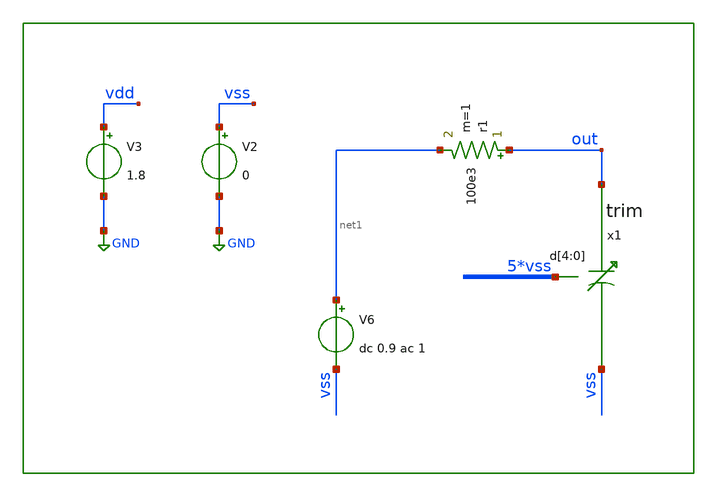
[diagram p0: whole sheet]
** sch_path: xschem/tb/comparator/ac_trim.sch
**.subckt ac_trim
V2 vss GND 0
V3 vdd GND 1.8
V6 net1 vss dc 0.9 ac 1
r1 out net1 100e3 m=1
x1 out vss vss vss vss vss vss trim
**** begin user architecture code

.param MC_SWITCH=0

.control
save all
ac dec 10 1 1e9

meas ac fbw when vdb(out)=-3
let ctrim = 1/(2*3.14159265*fbw*100e3)

print fbw
print ctrim

.endc


 * FET CORNERS
.include $::SKYWATER_MODELS/corners/tt.spice
*.include $::SKYWATER_MODELS/corners/ff.spice
*.include $::SKYWATER_MODELS/corners/ss.spice
*.include $::SKYWATER_MODELS/corners/sf.spice
*.include $::SKYWATER_MODELS/corners/fs.spice

* TT + R + C
*.include $::SKYWATER_MODELS/corners/tt_rmax_cmax.spice
*.include $::SKYWATER_MODELS/corners/tt_rmin_cmin.spice
*.include $::SKYWATER_MODELS/corners/tt_rmax_cmin.spice
*.include $::SKYWATER_MODELS/corners/tt_rmin_cmax.spice

* FF + R + C
*.include $::SKYWATER_MODELS/corners/ff_rmax_cmax.spice
*.include $::SKYWATER_MODELS/corners/ff_rmin_cmin.spice
*.include $::SKYWATER_MODELS/corners/ff_rmax_cmin.spice
*.include $::SKYWATER_MODELS/corners/ff_rmin_cmax.spice


* SS + R + C
*.include $::SKYWATER_MODELS/corners/ss_rmax_cmax.spice
*.include $::SKYWATER_MODELS/corners/ss_rmin_cmin.spice
*.include $::SKYWATER_MODELS/corners/ss_rmax_cmin.spice
*.include $::SKYWATER_MODELS/corners/ss_rmin_cmax.spice

* SF + R + C
*.include $::SKYWATER_MODELS/corners/sf_rmax_cmax.spice
*.include $::SKYWATER_MODELS/corners/sf_rmin_cmin.spice
*.include $::SKYWATER_MODELS/corners/sf_rmax_cmin.spice
*.include $::SKYWATER_MODELS/corners/sf_rmin_cmax.spice

* FS + R + C
*.include $::SKYWATER_MODELS/corners/fs_rmax_cmax.spice
*.include $::SKYWATER_MODELS/corners/fs_rmin_cmin.spice
*.include $::SKYWATER_MODELS/corners/fs_rmax_cmin.spice
*.include $::SKYWATER_MODELS/corners/fs_rmin_cmax.spice

**** end user architecture code
**.ends

* expanding   symbol:  sar_10b/comparator/trim.sym # of pins=3
** sym_path: xschem/sar_10b/comparator/trim.sym
** sch_path: xschem/sar_10b/comparator/trim.sch
.subckt trim drain d[4] d[3] d[2] d[1] d[0] vss
*.iopin vss
*.ipin d[4],d[3],d[2],d[1],d[0]
*.opin drain
XM4[7] n4 d[4] vss vss sky130_fd_pr__nfet_01v8_lvt L=0.3 W=1 nf=1 ad='int((nf+1)/2) * W/nf * 0.29' as='int((nf+2)/2) * W/nf * 0.29'
+ pd='2*int((nf+1)/2) * (W/nf + 0.29)' ps='2*int((nf+2)/2) * (W/nf + 0.29)' nrd='0.29 / W' nrs='0.29 / W'
+ sa=0 sb=0 sd=0 mult=1 m=1
XM4[6] n4 d[4] vss vss sky130_fd_pr__nfet_01v8_lvt L=0.3 W=1 nf=1 ad='int((nf+1)/2) * W/nf * 0.29' as='int((nf+2)/2) * W/nf * 0.29'
+ pd='2*int((nf+1)/2) * (W/nf + 0.29)' ps='2*int((nf+2)/2) * (W/nf + 0.29)' nrd='0.29 / W' nrs='0.29 / W'
+ sa=0 sb=0 sd=0 mult=1 m=1
XM4[5] n4 d[4] vss vss sky130_fd_pr__nfet_01v8_lvt L=0.3 W=1 nf=1 ad='int((nf+1)/2) * W/nf * 0.29' as='int((nf+2)/2) * W/nf * 0.29'
+ pd='2*int((nf+1)/2) * (W/nf + 0.29)' ps='2*int((nf+2)/2) * (W/nf + 0.29)' nrd='0.29 / W' nrs='0.29 / W'
+ sa=0 sb=0 sd=0 mult=1 m=1
XM4[4] n4 d[4] vss vss sky130_fd_pr__nfet_01v8_lvt L=0.3 W=1 nf=1 ad='int((nf+1)/2) * W/nf * 0.29' as='int((nf+2)/2) * W/nf * 0.29'
+ pd='2*int((nf+1)/2) * (W/nf + 0.29)' ps='2*int((nf+2)/2) * (W/nf + 0.29)' nrd='0.29 / W' nrs='0.29 / W'
+ sa=0 sb=0 sd=0 mult=1 m=1
XM4[3] n4 d[4] vss vss sky130_fd_pr__nfet_01v8_lvt L=0.3 W=1 nf=1 ad='int((nf+1)/2) * W/nf * 0.29' as='int((nf+2)/2) * W/nf * 0.29'
+ pd='2*int((nf+1)/2) * (W/nf + 0.29)' ps='2*int((nf+2)/2) * (W/nf + 0.29)' nrd='0.29 / W' nrs='0.29 / W'
+ sa=0 sb=0 sd=0 mult=1 m=1
XM4[2] n4 d[4] vss vss sky130_fd_pr__nfet_01v8_lvt L=0.3 W=1 nf=1 ad='int((nf+1)/2) * W/nf * 0.29' as='int((nf+2)/2) * W/nf * 0.29'
+ pd='2*int((nf+1)/2) * (W/nf + 0.29)' ps='2*int((nf+2)/2) * (W/nf + 0.29)' nrd='0.29 / W' nrs='0.29 / W'
+ sa=0 sb=0 sd=0 mult=1 m=1
XM4[1] n4 d[4] vss vss sky130_fd_pr__nfet_01v8_lvt L=0.3 W=1 nf=1 ad='int((nf+1)/2) * W/nf * 0.29' as='int((nf+2)/2) * W/nf * 0.29'
+ pd='2*int((nf+1)/2) * (W/nf + 0.29)' ps='2*int((nf+2)/2) * (W/nf + 0.29)' nrd='0.29 / W' nrs='0.29 / W'
+ sa=0 sb=0 sd=0 mult=1 m=1
XM4[0] n4 d[4] vss vss sky130_fd_pr__nfet_01v8_lvt L=0.3 W=1 nf=1 ad='int((nf+1)/2) * W/nf * 0.29' as='int((nf+2)/2) * W/nf * 0.29'
+ pd='2*int((nf+1)/2) * (W/nf + 0.29)' ps='2*int((nf+2)/2) * (W/nf + 0.29)' nrd='0.29 / W' nrs='0.29 / W'
+ sa=0 sb=0 sd=0 mult=1 m=1
XM3[3] n3 d[3] vss vss sky130_fd_pr__nfet_01v8_lvt L=0.3 W=1 nf=1 ad='int((nf+1)/2) * W/nf * 0.29' as='int((nf+2)/2) * W/nf * 0.29'
+ pd='2*int((nf+1)/2) * (W/nf + 0.29)' ps='2*int((nf+2)/2) * (W/nf + 0.29)' nrd='0.29 / W' nrs='0.29 / W'
+ sa=0 sb=0 sd=0 mult=1 m=1
XM3[2] n3 d[3] vss vss sky130_fd_pr__nfet_01v8_lvt L=0.3 W=1 nf=1 ad='int((nf+1)/2) * W/nf * 0.29' as='int((nf+2)/2) * W/nf * 0.29'
+ pd='2*int((nf+1)/2) * (W/nf + 0.29)' ps='2*int((nf+2)/2) * (W/nf + 0.29)' nrd='0.29 / W' nrs='0.29 / W'
+ sa=0 sb=0 sd=0 mult=1 m=1
XM3[1] n3 d[3] vss vss sky130_fd_pr__nfet_01v8_lvt L=0.3 W=1 nf=1 ad='int((nf+1)/2) * W/nf * 0.29' as='int((nf+2)/2) * W/nf * 0.29'
+ pd='2*int((nf+1)/2) * (W/nf + 0.29)' ps='2*int((nf+2)/2) * (W/nf + 0.29)' nrd='0.29 / W' nrs='0.29 / W'
+ sa=0 sb=0 sd=0 mult=1 m=1
XM3[0] n3 d[3] vss vss sky130_fd_pr__nfet_01v8_lvt L=0.3 W=1 nf=1 ad='int((nf+1)/2) * W/nf * 0.29' as='int((nf+2)/2) * W/nf * 0.29'
+ pd='2*int((nf+1)/2) * (W/nf + 0.29)' ps='2*int((nf+2)/2) * (W/nf + 0.29)' nrd='0.29 / W' nrs='0.29 / W'
+ sa=0 sb=0 sd=0 mult=1 m=1
XM2[1] n2 d[2] vss vss sky130_fd_pr__nfet_01v8_lvt L=0.3 W=1 nf=1 ad='int((nf+1)/2) * W/nf * 0.29' as='int((nf+2)/2) * W/nf * 0.29'
+ pd='2*int((nf+1)/2) * (W/nf + 0.29)' ps='2*int((nf+2)/2) * (W/nf + 0.29)' nrd='0.29 / W' nrs='0.29 / W'
+ sa=0 sb=0 sd=0 mult=1 m=1
XM2[0] n2 d[2] vss vss sky130_fd_pr__nfet_01v8_lvt L=0.3 W=1 nf=1 ad='int((nf+1)/2) * W/nf * 0.29' as='int((nf+2)/2) * W/nf * 0.29'
+ pd='2*int((nf+1)/2) * (W/nf + 0.29)' ps='2*int((nf+2)/2) * (W/nf + 0.29)' nrd='0.29 / W' nrs='0.29 / W'
+ sa=0 sb=0 sd=0 mult=1 m=1
XM1 n1 d[1] vss vss sky130_fd_pr__nfet_01v8_lvt L=0.3 W=1 nf=1 ad='int((nf+1)/2) * W/nf * 0.29' as='int((nf+2)/2) * W/nf * 0.29'
+ pd='2*int((nf+1)/2) * (W/nf + 0.29)' ps='2*int((nf+2)/2) * (W/nf + 0.29)' nrd='0.29 / W' nrs='0.29 / W'
+ sa=0 sb=0 sd=0 mult=1 m=1
XM0 n0 d[0] vss vss sky130_fd_pr__nfet_01v8_lvt L=0.3 W=1 nf=1 ad='int((nf+1)/2) * W/nf * 0.29' as='int((nf+2)/2) * W/nf * 0.29'
+ pd='2*int((nf+1)/2) * (W/nf + 0.29)' ps='2*int((nf+2)/2) * (W/nf + 0.29)' nrd='0.29 / W' nrs='0.29 / W'
+ sa=0 sb=0 sd=0 mult=1 m=1
x4[7] drain n4 trimcap
x4[6] drain n4 trimcap
x4[5] drain n4 trimcap
x4[4] drain n4 trimcap
x4[3] drain n4 trimcap
x4[2] drain n4 trimcap
x4[1] drain n4 trimcap
x4[0] drain n4 trimcap
x3[3] drain n3 trimcap
x3[2] drain n3 trimcap
x3[1] drain n3 trimcap
x3[0] drain n3 trimcap
x2[1] drain n2 trimcap
x2[0] drain n2 trimcap
x1 drain n1 trimcap
x0 drain n0 trimcap
.ends


* expanding   symbol:  sar_10b/comparator/trimcap.sym # of pins=2
** sym_path: xschem/sar_10b/comparator/trimcap.sym
** sch_path: xschem/sar_10b/comparator/trimcap.sch
.subckt trimcap cp cn
*.iopin cp
*.iopin cn
c0 net1 cn 2f m=1
c1 cp net1 1f m=1
.ends

.GLOBAL GND
.end
